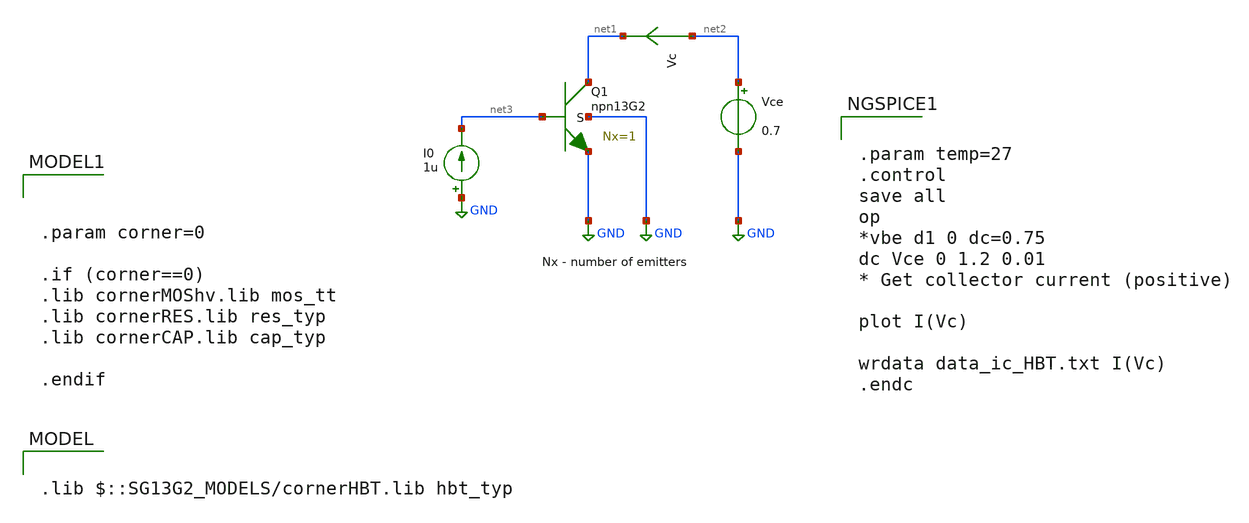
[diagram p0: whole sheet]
** sch_path: DelayLine/others/single mos/tb_HBT_charac.sch
**.subckt tb_HBT_charac
Vce net2 GND 0.7
Vc net2 net1 0
.save i(vc)
XQ1 net1 net3 GND GND npn13G2 Nx=1 mm_ok=1
I0 GND net3 1u
**** begin user architecture code


.param corner=0

.if (corner==0)
.lib cornerMOShv.lib mos_tt
.lib cornerRES.lib res_typ
.lib cornerCAP.lib cap_typ

.endif


.lib $::SG13G2_MODELS/cornerHBT.lib hbt_typ



.param temp=27
.control
save all
op
*vbe d1 0 dc=0.75
dc Vce 0 1.2 0.01
* Get collector current (positive)

plot I(Vc)

wrdata data_ic_HBT.txt I(Vc)
.endc


**** end user architecture code
**.ends
.GLOBAL GND
.end
